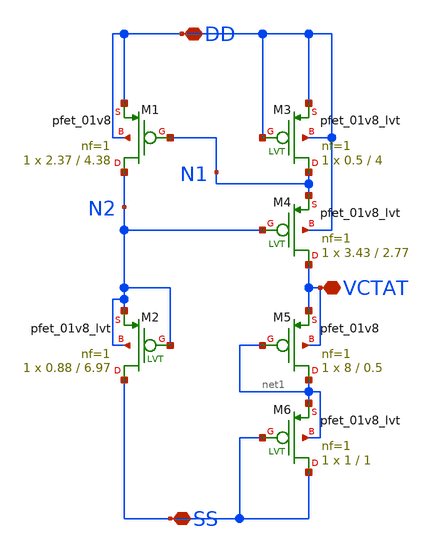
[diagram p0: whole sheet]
** sch_path: xschem/iref_2nA_vref_v2.sch
**.subckt iref_2nA_vref_v2 DD SS VCTAT
*.iopin DD
*.iopin SS
*.iopin VCTAT
XM1 N2 N1 DD DD sky130_fd_pr__pfet_01v8 L=4.38 W=2.37 nf=1 ad='int((nf+1)/2) * W/nf * 0.29' as='int((nf+2)/2) * W/nf * 0.29'
+ pd='2*int((nf+1)/2) * (W/nf + 0.29)' ps='2*int((nf+2)/2) * (W/nf + 0.29)' nrd='0.29 / W' nrs='0.29 / W'
+ sa=0 sb=0 sd=0 mult=1 m=1
XM2 SS N2 N2 N2 sky130_fd_pr__pfet_01v8_lvt L=6.97 W=0.88 nf=1 ad='int((nf+1)/2) * W/nf * 0.29' as='int((nf+2)/2) * W/nf * 0.29'
+ pd='2*int((nf+1)/2) * (W/nf + 0.29)' ps='2*int((nf+2)/2) * (W/nf + 0.29)' nrd='0.29 / W' nrs='0.29 / W'
+ sa=0 sb=0 sd=0 mult=1 m=1
XM3 N1 DD DD DD sky130_fd_pr__pfet_01v8_lvt L=4 W=0.5 nf=1 ad='int((nf+1)/2) * W/nf * 0.29' as='int((nf+2)/2) * W/nf * 0.29'
+ pd='2*int((nf+1)/2) * (W/nf + 0.29)' ps='2*int((nf+2)/2) * (W/nf + 0.29)' nrd='0.29 / W' nrs='0.29 / W'
+ sa=0 sb=0 sd=0 mult=1 m=1
XM4 VCTAT N2 N1 DD sky130_fd_pr__pfet_01v8_lvt L=2.77 W=3.43 nf=1 ad='int((nf+1)/2) * W/nf * 0.29' as='int((nf+2)/2) * W/nf * 0.29'
+ pd='2*int((nf+1)/2) * (W/nf + 0.29)' ps='2*int((nf+2)/2) * (W/nf + 0.29)' nrd='0.29 / W' nrs='0.29 / W'
+ sa=0 sb=0 sd=0 mult=1 m=1
XM5 net1 net1 VCTAT VCTAT sky130_fd_pr__pfet_01v8 L=0.5 W=8 nf=1 ad='int((nf+1)/2) * W/nf * 0.29' as='int((nf+2)/2) * W/nf * 0.29'
+ pd='2*int((nf+1)/2) * (W/nf + 0.29)' ps='2*int((nf+2)/2) * (W/nf + 0.29)' nrd='0.29 / W' nrs='0.29 / W'
+ sa=0 sb=0 sd=0 mult=1 m=1
XM6 SS SS net1 net1 sky130_fd_pr__pfet_01v8_lvt L=1 W=1 nf=1 ad='int((nf+1)/2) * W/nf * 0.29' as='int((nf+2)/2) * W/nf * 0.29'
+ pd='2*int((nf+1)/2) * (W/nf + 0.29)' ps='2*int((nf+2)/2) * (W/nf + 0.29)' nrd='0.29 / W' nrs='0.29 / W'
+ sa=0 sb=0 sd=0 mult=1 m=1
**.ends
.end
